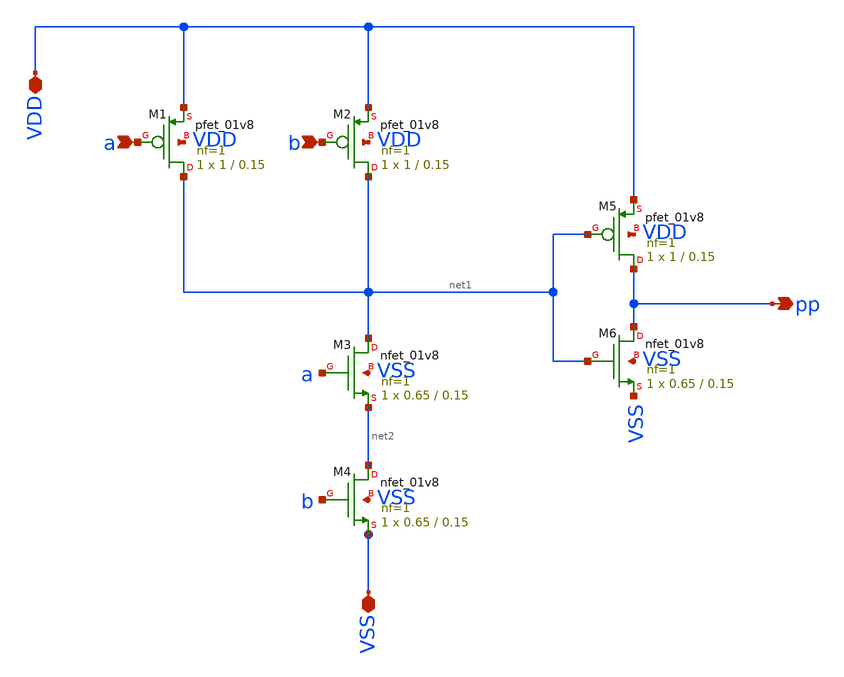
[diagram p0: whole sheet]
** sch_path: xschem/and2.sch
**.subckt and2 pp VDD VSS a b
*.opin pp
*.iopin VDD
*.iopin VSS
*.ipin a
*.ipin b
XM1 net1 a VDD VDD sky130_fd_pr__pfet_01v8 L=0.15 W=1 nf=1 ad='int((1 + 1)/2) * 1 / 1 * 0.29' as='int((1 + 2)/2) * 1 / 1 * 0.29'
+ pd='2*int((1 + 1)/2) * (1 / 1 + 0.29)' ps='2*int((1 + 2)/2) * (1 / 1 + 0.29)' nrd='0.29 / 1 ' nrs='0.29 / 1 '
+ sa=0 sb=0 sd=0 mult=1 m=1
XM2 net1 b VDD VDD sky130_fd_pr__pfet_01v8 L=0.15 W=1 nf=1 ad='int((1 + 1)/2) * 1 / 1 * 0.29' as='int((1 + 2)/2) * 1 / 1 * 0.29'
+ pd='2*int((1 + 1)/2) * (1 / 1 + 0.29)' ps='2*int((1 + 2)/2) * (1 / 1 + 0.29)' nrd='0.29 / 1 ' nrs='0.29 / 1 '
+ sa=0 sb=0 sd=0 mult=1 m=1
XM3 net1 a net2 VSS sky130_fd_pr__nfet_01v8 L=0.15 W=0.65 nf=1 ad='int((1 + 1)/2) * 0.65 / 1 * 0.29'
+ as='int((1 + 2)/2) * 0.65 / 1 * 0.29' pd='2*int((1 + 1)/2) * (0.65 / 1 + 0.29)' ps='2*int((1 + 2)/2) * (0.65 / 1 + 0.29)'
+ nrd='0.29 / 0.65 ' nrs='0.29 / 0.65 ' sa=0 sb=0 sd=0 mult=1 m=1
XM4 net2 b VSS VSS sky130_fd_pr__nfet_01v8 L=0.15 W=0.65 nf=1 ad='int((1 + 1)/2) * 0.65 / 1 * 0.29' as='int((1 + 2)/2) * 0.65 / 1 * 0.29'
+ pd='2*int((1 + 1)/2) * (0.65 / 1 + 0.29)' ps='2*int((1 + 2)/2) * (0.65 / 1 + 0.29)' nrd='0.29 / 0.65 '
+ nrs='0.29 / 0.65 ' sa=0 sb=0 sd=0 mult=1 m=1
XM5 pp net1 VDD VDD sky130_fd_pr__pfet_01v8 L=0.15 W=1 nf=1 ad='int((1 + 1)/2) * 1 / 1 * 0.29' as='int((1 + 2)/2) * 1 / 1 * 0.29'
+ pd='2*int((1 + 1)/2) * (1 / 1 + 0.29)' ps='2*int((1 + 2)/2) * (1 / 1 + 0.29)' nrd='0.29 / 1 ' nrs='0.29 / 1 '
+ sa=0 sb=0 sd=0 mult=1 m=1
XM6 pp net1 VSS VSS sky130_fd_pr__nfet_01v8 L=0.15 W=0.65 nf=1 ad='int((1 + 1)/2) * 0.65 / 1 * 0.29'
+ as='int((1 + 2)/2) * 0.65 / 1 * 0.29' pd='2*int((1 + 1)/2) * (0.65 / 1 + 0.29)' ps='2*int((1 + 2)/2) * (0.65 / 1 + 0.29)'
+ nrd='0.29 / 0.65 ' nrs='0.29 / 0.65 ' sa=0 sb=0 sd=0 mult=1 m=1
**.ends
.end
